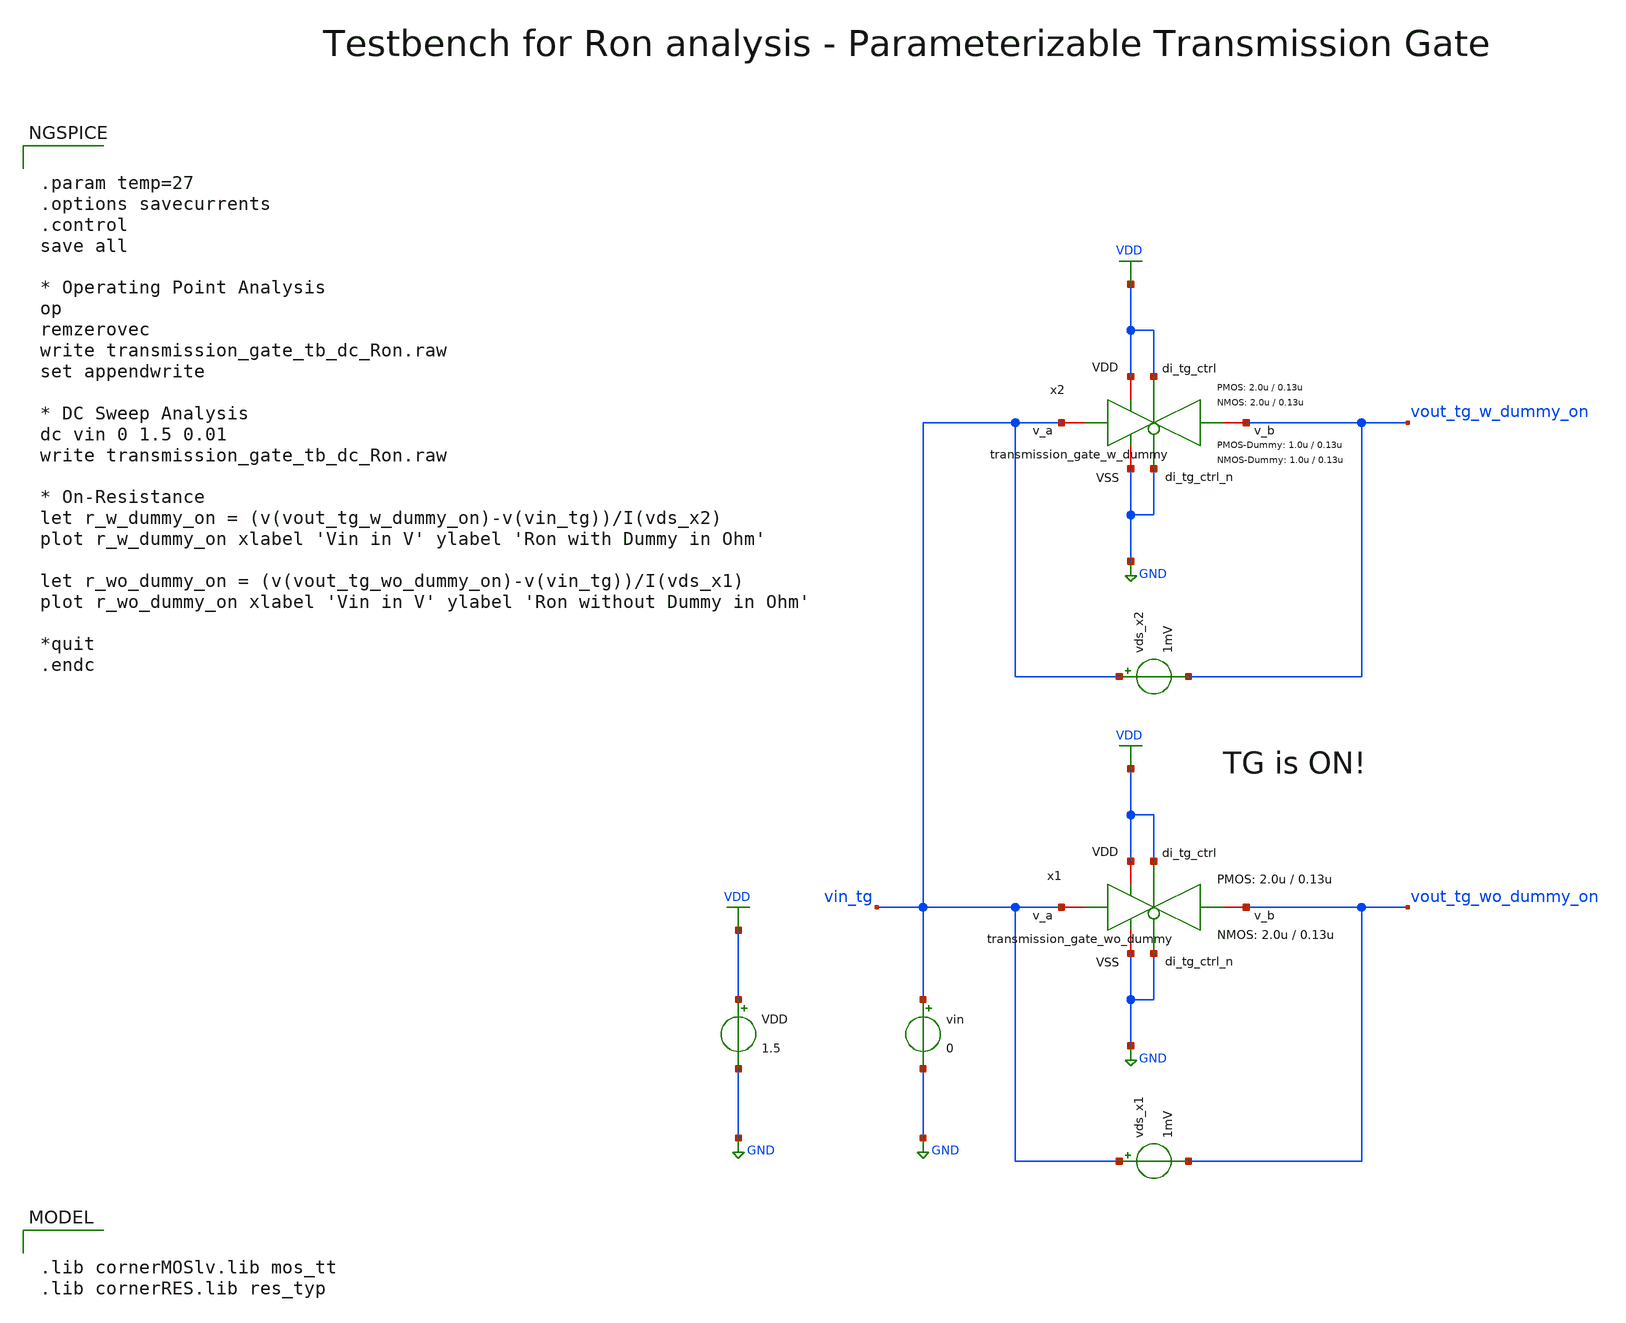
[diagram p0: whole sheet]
** sch_path: xschem/transmission_gate/testbenches/transmission_gate_tb_dc_Ron.sch
**.subckt transmission_gate_tb_dc_Ron
VDD VDD GND 1.5
vin vin_tg GND 0
vds_x1 vin_tg vout_tg_wo_dummy_on 1mV
x1 VDD VDD GND vout_tg_wo_dummy_on vin_tg GND transmission_gate_wo_dummy W_P=2.0u L_P=0.13u W_N=2.0u
+ L_N=0.13u
vds_x2 vin_tg vout_tg_w_dummy_on 1mV
x2 VDD VDD GND vout_tg_w_dummy_on vin_tg GND transmission_gate_w_dummy W_P=2.0u L_P=0.13u W_N=2.0u
+ L_N=0.13u W_P_D=1.0u L_P_D=0.13u W_N_D=1.0u L_N_D=0.13u
**** begin user architecture code

.lib cornerMOSlv.lib mos_tt
.lib cornerRES.lib res_typ



.param temp=27
.options savecurrents
.control
save all

* Operating Point Analysis
op
remzerovec
write transmission_gate_tb_dc_Ron.raw
set appendwrite

* DC Sweep Analysis
dc vin 0 1.5 0.01
write transmission_gate_tb_dc_Ron.raw

* On-Resistance
let r_w_dummy_on = (v(vout_tg_w_dummy_on)-v(vin_tg))/I(vds_x2)
plot r_w_dummy_on xlabel 'Vin in V' ylabel 'Ron with Dummy in Ohm'

let r_wo_dummy_on = (v(vout_tg_wo_dummy_on)-v(vin_tg))/I(vds_x1)
plot r_wo_dummy_on xlabel 'Vin in V' ylabel 'Ron without Dummy in Ohm'

*quit
.endc

**** end user architecture code
**.ends

* expanding   symbol:  transmission_gate/transmission_gate_wo_dummy.sym # of pins=6
** sym_path: xschem/transmission_gate/transmission_gate_wo_dummy.sym
** sch_path: xschem/transmission_gate/transmission_gate_wo_dummy.sch
.subckt transmission_gate_wo_dummy VDD di_tg_ctrl VSS v_b v_a di_tg_ctrl_n  W_P=3.0u L_P=0.13u
+ W_N=1.0u L_N=0.13u
*.iopin v_a
*.iopin v_b
*.iopin VDD
*.iopin VSS
*.ipin di_tg_ctrl
*.ipin di_tg_ctrl_n
XM1 v_b di_tg_ctrl v_a VSS sg13_lv_nmos w=W_N l=L_N ng=1 m=1 mm_ok=1
XM2 v_a di_tg_ctrl_n v_b VDD sg13_lv_pmos w=W_P l=L_P ng=1 m=1 mm_ok=1
.ends


* expanding   symbol:  transmission_gate/transmission_gate_w_dummy.sym # of pins=6
** sym_path: xschem/transmission_gate/transmission_gate_w_dummy.sym
** sch_path: xschem/transmission_gate/transmission_gate_w_dummy.sch
.subckt transmission_gate_w_dummy VDD di_tg_ctrl VSS v_b v_a di_tg_ctrl_n  W_P=2.0u L_P=0.13u
+ W_N=2.0u L_N=0.13u W_P_D=1.0u L_P_D=0.13u W_N_D=1.0u L_N_D=0.13u
*.iopin v_a
*.iopin v_b
*.iopin VDD
*.iopin VSS
*.ipin di_tg_ctrl
*.ipin di_tg_ctrl_n
XM1 v_b di_tg_ctrl v_a VSS sg13_lv_nmos w=W_N l=L_N ng=1 m=1 mm_ok=1
XM2 v_a di_tg_ctrl_n v_b VDD sg13_lv_pmos w=W_P l=L_P ng=1 m=1 mm_ok=1
XMdummy2 v_b di_tg_ctrl v_b VDD sg13_lv_pmos w=W_P_D l=L_P_D ng=1 m=1 mm_ok=1
XMdummy1 v_b di_tg_ctrl_n v_b VSS sg13_lv_nmos w=W_N_D l=L_N_D ng=1 m=1 mm_ok=1
.ends

.GLOBAL GND
.GLOBAL VDD
.end
